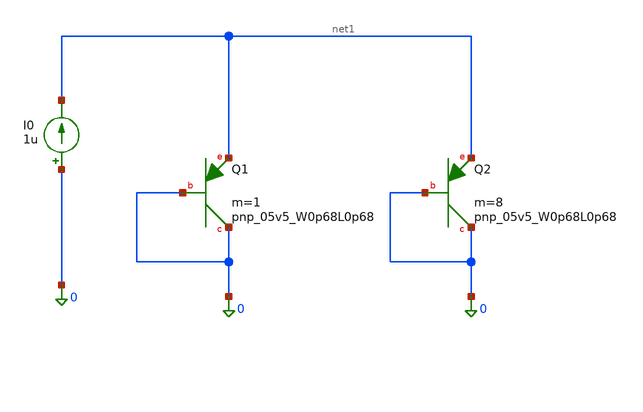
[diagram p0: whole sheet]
** sch_path: designs/bgr_ldo/src/bgr.sch
**.subckt bgr
XQ1 0 0 net1 sky130_fd_pr__pnp_05v5_W0p68L0p68 m=1
XQ2 0 0 net1 sky130_fd_pr__pnp_05v5_W0p68L0p68 m=8
I0 0 net1 1u
**.ends
.end
